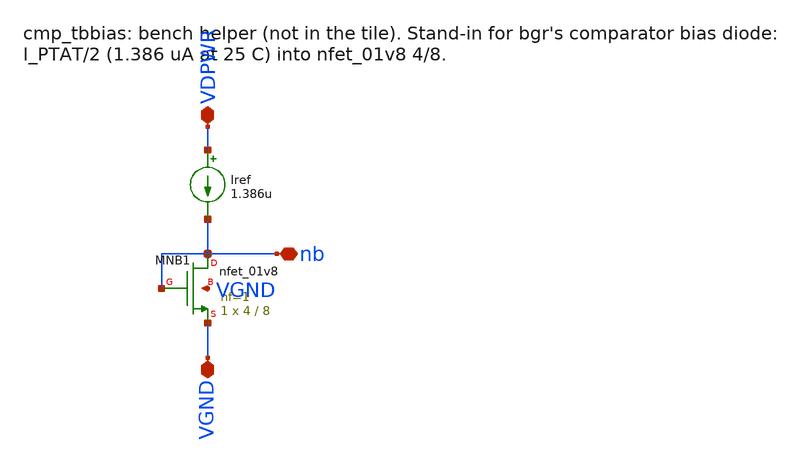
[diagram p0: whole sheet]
** sch_path: xschem/cmp_tbbias.sch
**.subckt cmp_tbbias VDPWR nb VGND
*.iopin VDPWR
*.iopin nb
*.iopin VGND
Iref VDPWR nb 1.386u
XMNB1 nb nb VGND VGND sky130_fd_pr__nfet_01v8 L=8 W=4 nf=1 ad='int((1 + 1)/2) * 4 / 1 * 0.29' as='int((1 + 2)/2) * 4 / 1 * 0.29'
+ pd='2*int((1 + 1)/2) * (4 / 1 + 0.29)' ps='2*int((1 + 2)/2) * (4 / 1 + 0.29)' nrd='0.29 / 4 ' nrs='0.29 / 4 '
+ sa=0 sb=0 sd=0 mult=1 m=1
**.ends
.end
